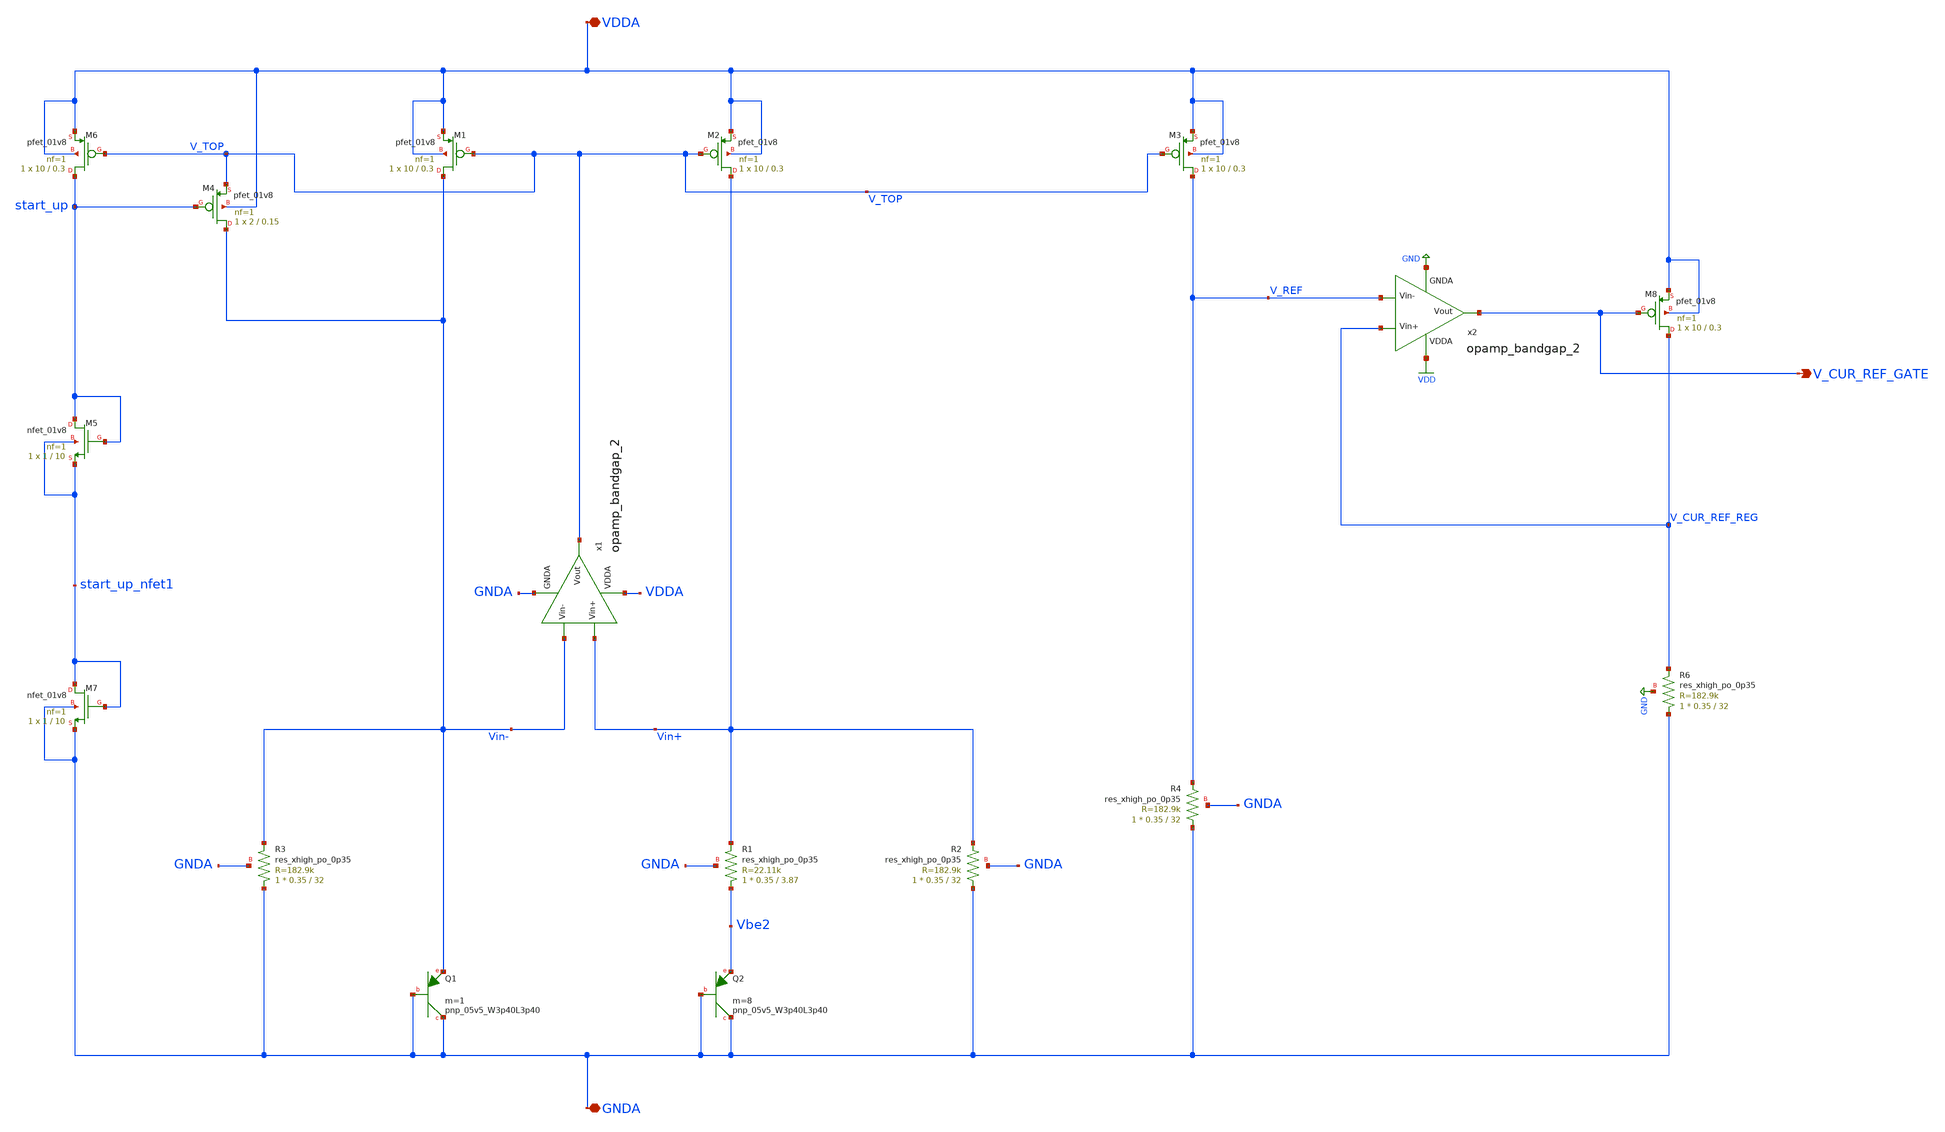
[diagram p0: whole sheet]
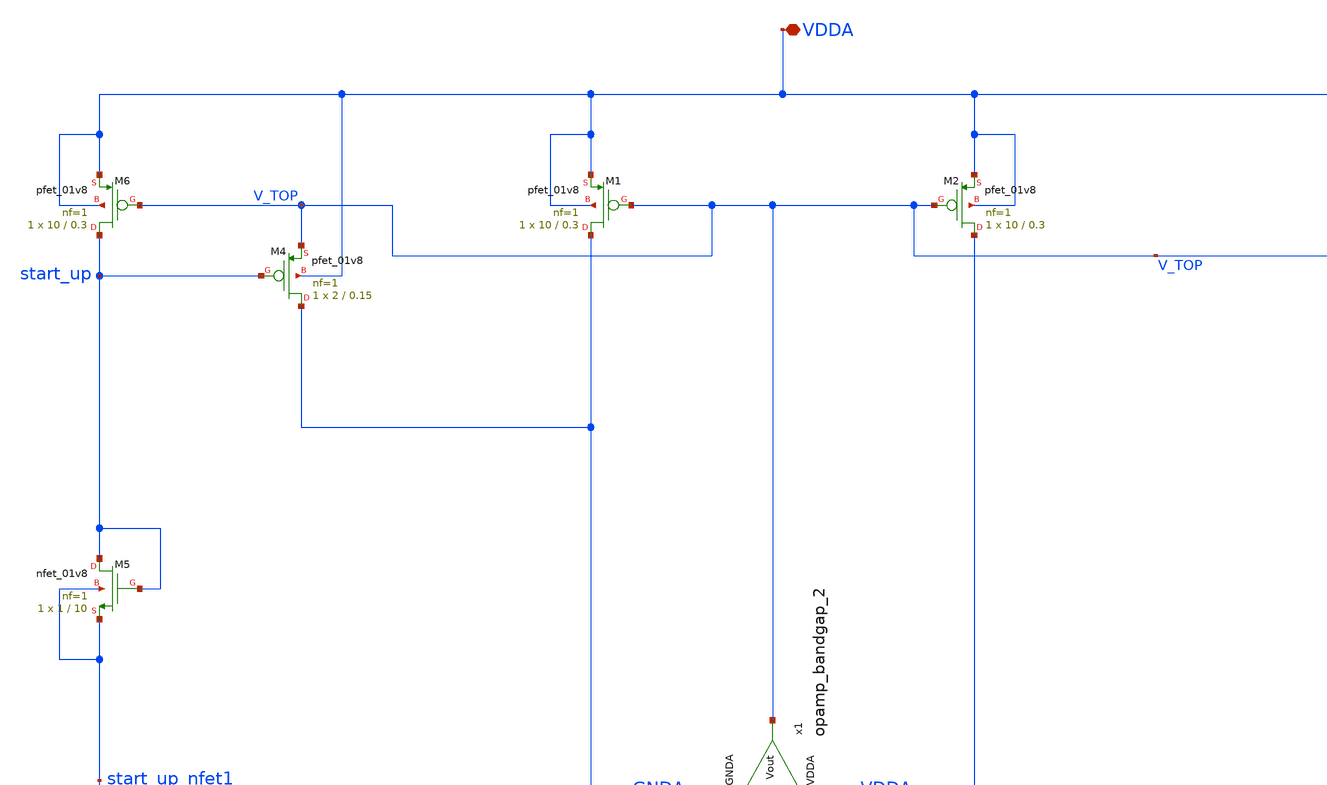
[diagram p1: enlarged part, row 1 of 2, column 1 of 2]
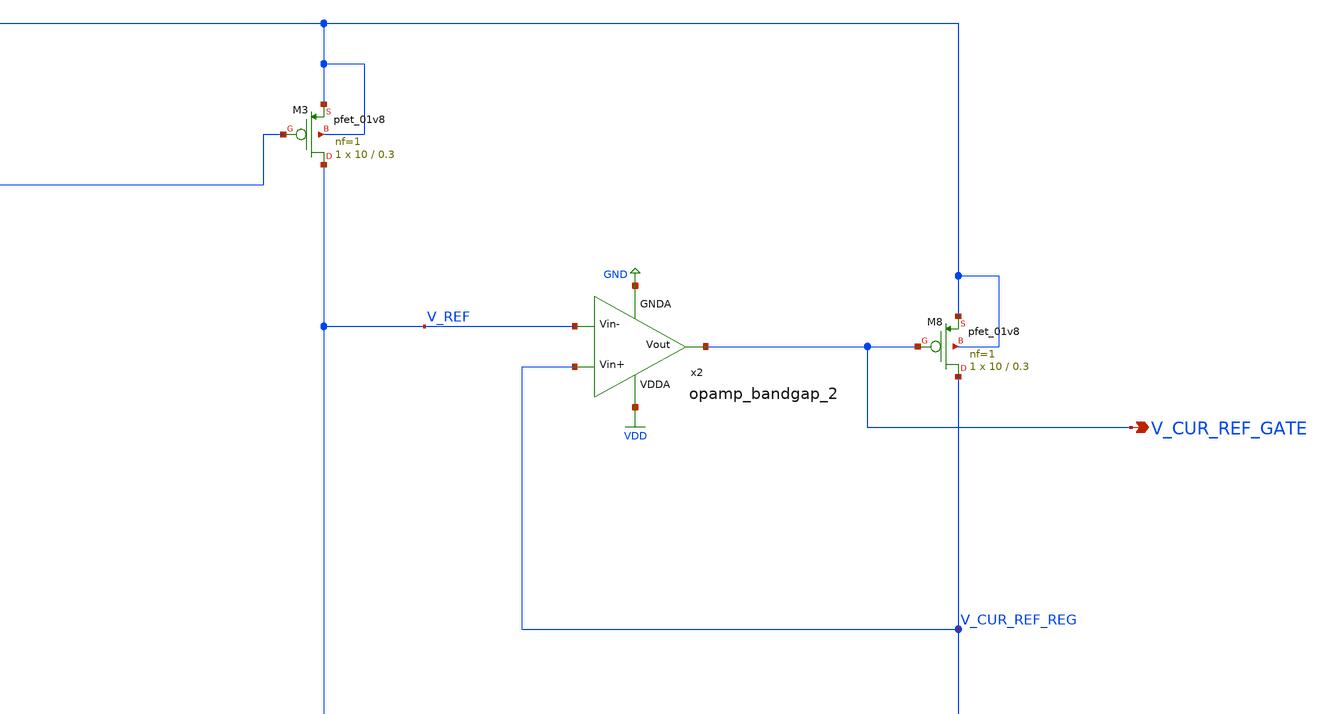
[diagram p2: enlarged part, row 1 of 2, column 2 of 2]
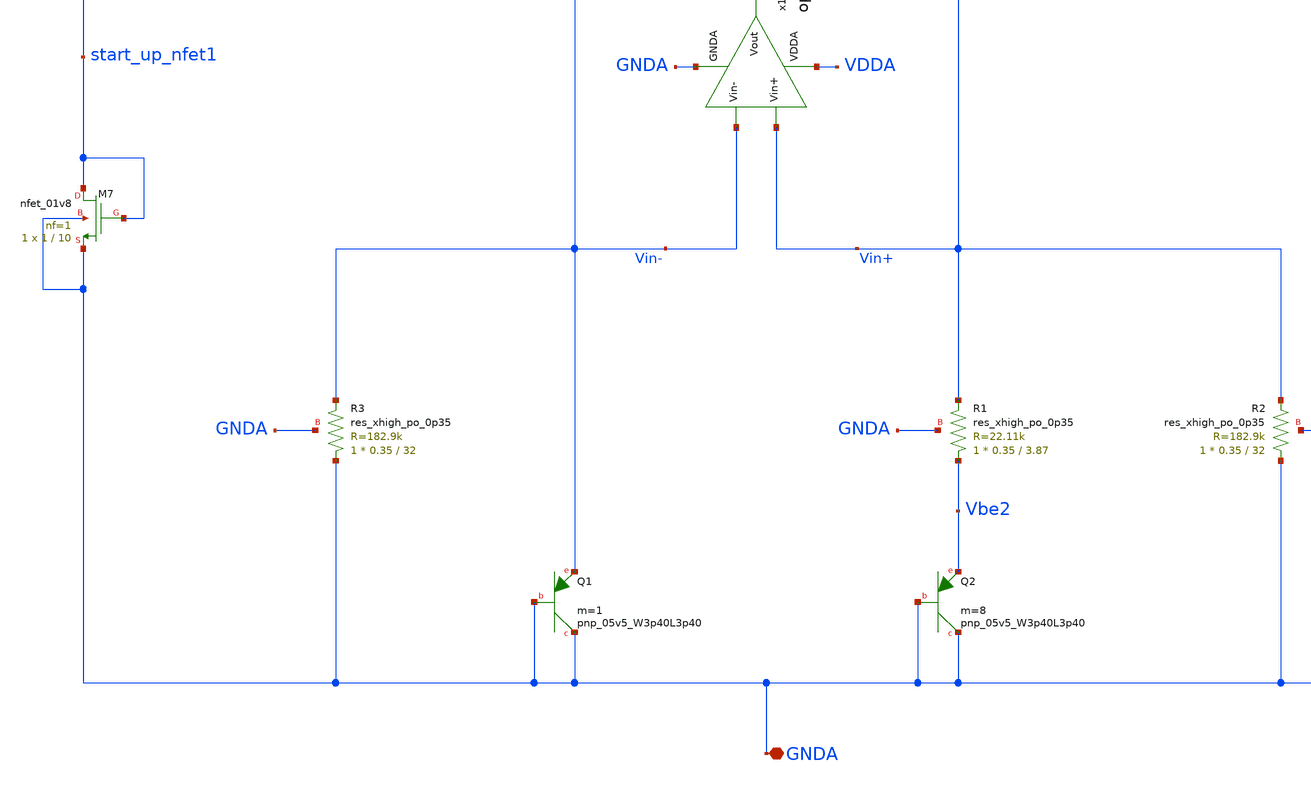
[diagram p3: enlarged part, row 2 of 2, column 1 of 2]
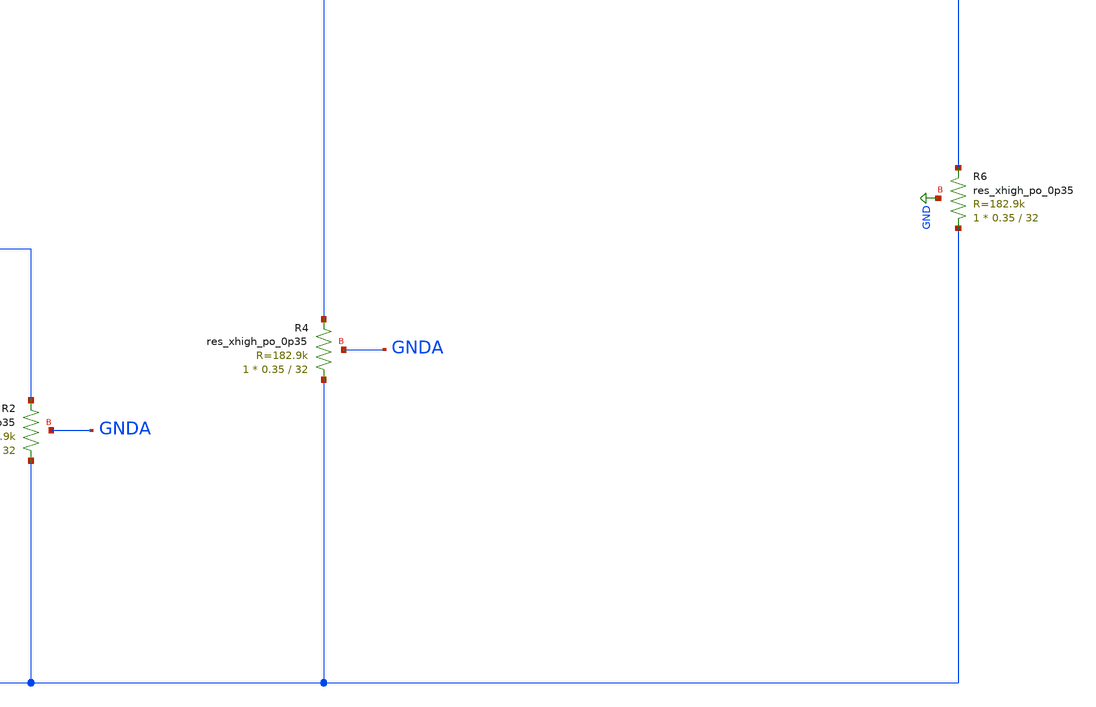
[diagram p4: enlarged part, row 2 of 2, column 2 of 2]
** sch_path: projects/bandgapref/xschem_ngspice/new_files/current_gen_5uA.sch
**.subckt current_gen_5uA VDDA GNDA V_CUR_REF_GATE
*.iopin VDDA
*.iopin GNDA
*.opin V_CUR_REF_GATE
XQ1 GNDA GNDA Vin- sky130_fd_pr__pnp_05v5_W3p40L3p40 m=1
XQ2 GNDA GNDA Vbe2 sky130_fd_pr__pnp_05v5_W3p40L3p40 m=8
XM1 Vin- V_TOP VDDA VDDA sky130_fd_pr__pfet_01v8 L=0.3 W=10 nf=1 ad='int((nf+1)/2) * W/nf * 0.29' as='int((nf+2)/2) * W/nf * 0.29'
+ pd='2*int((nf+1)/2) * (W/nf + 0.29)' ps='2*int((nf+2)/2) * (W/nf + 0.29)' nrd='0.29 / W' nrs='0.29 / W'
+ sa=0 sb=0 sd=0 mult=1 m=1
XM2 Vin+ V_TOP VDDA VDDA sky130_fd_pr__pfet_01v8 L=0.3 W=10 nf=1 ad='int((nf+1)/2) * W/nf * 0.29' as='int((nf+2)/2) * W/nf * 0.29'
+ pd='2*int((nf+1)/2) * (W/nf + 0.29)' ps='2*int((nf+2)/2) * (W/nf + 0.29)' nrd='0.29 / W' nrs='0.29 / W'
+ sa=0 sb=0 sd=0 mult=1 m=1
XM3 V_REF V_TOP VDDA VDDA sky130_fd_pr__pfet_01v8 L=0.3 W=10 nf=1 ad='int((nf+1)/2) * W/nf * 0.29' as='int((nf+2)/2) * W/nf * 0.29'
+ pd='2*int((nf+1)/2) * (W/nf + 0.29)' ps='2*int((nf+2)/2) * (W/nf + 0.29)' nrd='0.29 / W' nrs='0.29 / W'
+ sa=0 sb=0 sd=0 mult=1 m=1
XR1 Vbe2 Vin+ GNDA sky130_fd_pr__res_xhigh_po_0p35 L=3.87 mult=1 m=1
XR2 GNDA Vin+ GNDA sky130_fd_pr__res_xhigh_po_0p35 L=32 mult=1 m=1
XR3 GNDA Vin- GNDA sky130_fd_pr__res_xhigh_po_0p35 L=32 mult=1 m=1
XR4 GNDA V_REF GNDA sky130_fd_pr__res_xhigh_po_0p35 L=32 mult=1 m=1
XM5 start_up start_up start_up_nfet1 start_up_nfet1 sky130_fd_pr__nfet_01v8 L=10 W=1 nf=1 ad='int((nf+1)/2) * W/nf * 0.29'
+ as='int((nf+2)/2) * W/nf * 0.29' pd='2*int((nf+1)/2) * (W/nf + 0.29)' ps='2*int((nf+2)/2) * (W/nf + 0.29)'
+ nrd='0.29 / W' nrs='0.29 / W' sa=0 sb=0 sd=0 mult=1 m=1
XM6 start_up V_TOP VDDA VDDA sky130_fd_pr__pfet_01v8 L=0.3 W=10 nf=1 ad='int((nf+1)/2) * W/nf * 0.29'
+ as='int((nf+2)/2) * W/nf * 0.29' pd='2*int((nf+1)/2) * (W/nf + 0.29)' ps='2*int((nf+2)/2) * (W/nf + 0.29)'
+ nrd='0.29 / W' nrs='0.29 / W' sa=0 sb=0 sd=0 mult=1 m=1
XM4 Vin- start_up V_TOP VDDA sky130_fd_pr__pfet_01v8 L=0.15 W=2 nf=1 ad='int((nf+1)/2) * W/nf * 0.29'
+ as='int((nf+2)/2) * W/nf * 0.29' pd='2*int((nf+1)/2) * (W/nf + 0.29)' ps='2*int((nf+2)/2) * (W/nf + 0.29)'
+ nrd='0.29 / W' nrs='0.29 / W' sa=0 sb=0 sd=0 mult=1 m=1
x1 VDDA V_TOP Vin- Vin+ GNDA opamp_bandgap_2
XM7 start_up_nfet1 start_up_nfet1 GNDA GNDA sky130_fd_pr__nfet_01v8 L=10 W=1 nf=1 ad='int((nf+1)/2) * W/nf * 0.29'
+ as='int((nf+2)/2) * W/nf * 0.29' pd='2*int((nf+1)/2) * (W/nf + 0.29)' ps='2*int((nf+2)/2) * (W/nf + 0.29)'
+ nrd='0.29 / W' nrs='0.29 / W' sa=0 sb=0 sd=0 mult=1 m=1
x2 VDD V_CUR_REF_GATE V_REF V_CUR_REF_REG GND opamp_bandgap_2
XR6 GNDA V_CUR_REF_REG GND sky130_fd_pr__res_xhigh_po_0p35 L=32 mult=1 m=1
XM8 V_CUR_REF_REG V_CUR_REF_GATE VDDA VDDA sky130_fd_pr__pfet_01v8 L=0.3 W=10 nf=1 ad='int((nf+1)/2) * W/nf * 0.29'
+ as='int((nf+2)/2) * W/nf * 0.29' pd='2*int((nf+1)/2) * (W/nf + 0.29)' ps='2*int((nf+2)/2) * (W/nf + 0.29)'
+ nrd='0.29 / W' nrs='0.29 / W' sa=0 sb=0 sd=0 mult=1 m=1
**.ends

* expanding   symbol:  opamp_bandgap_2.sym # of pins=5
** sym_path: projects/bandgapref/xschem_ngspice/new_files/opamp_bandgap_2.sym
** sch_path: projects/bandgapref/xschem_ngspice/new_files/opamp_bandgap_2.sch
.subckt opamp_bandgap_2 VDDA Vout Vin- Vin+ GNDA
*.ipin Vin+
*.opin Vout
*.ipin Vin-
*.ipin GNDA
*.ipin VDDA
XM1 V_p VDDA GNDA GNDA sky130_fd_pr__nfet_01v8 L=10 W=5 nf=1 ad='int((nf+1)/2) * W/nf * 0.29' as='int((nf+2)/2) * W/nf * 0.29'
+ pd='2*int((nf+1)/2) * (W/nf + 0.29)' ps='2*int((nf+2)/2) * (W/nf + 0.29)' nrd='0.29 / W' nrs='0.29 / W'
+ sa=0 sb=0 sd=0 mult=1 m=1
XM2 V_mirror Vin- V_p GNDA sky130_fd_pr__nfet_01v8 L=0.2 W=5 nf=1 ad='int((nf+1)/2) * W/nf * 0.29' as='int((nf+2)/2) * W/nf * 0.29'
+ pd='2*int((nf+1)/2) * (W/nf + 0.29)' ps='2*int((nf+2)/2) * (W/nf + 0.29)' nrd='0.29 / W' nrs='0.29 / W'
+ sa=0 sb=0 sd=0 mult=1 m=1
XM3 1st_Vout Vin+ V_p GNDA sky130_fd_pr__nfet_01v8 L=0.2 W=5 nf=1 ad='int((nf+1)/2) * W/nf * 0.29' as='int((nf+2)/2) * W/nf * 0.29'
+ pd='2*int((nf+1)/2) * (W/nf + 0.29)' ps='2*int((nf+2)/2) * (W/nf + 0.29)' nrd='0.29 / W' nrs='0.29 / W'
+ sa=0 sb=0 sd=0 mult=1 m=1
XM5 V_mirror V_mirror VDDA VDDA sky130_fd_pr__pfet_01v8 L=0.2 W=10 nf=2 ad='int((nf+1)/2) * W/nf * 0.29'
+ as='int((nf+2)/2) * W/nf * 0.29' pd='2*int((nf+1)/2) * (W/nf + 0.29)' ps='2*int((nf+2)/2) * (W/nf + 0.29)'
+ nrd='0.29 / W' nrs='0.29 / W' sa=0 sb=0 sd=0 mult=1 m=1
XM6 1st_Vout V_mirror VDDA VDDA sky130_fd_pr__pfet_01v8 L=0.2 W=10 nf=2 ad='int((nf+1)/2) * W/nf * 0.29'
+ as='int((nf+2)/2) * W/nf * 0.29' pd='2*int((nf+1)/2) * (W/nf + 0.29)' ps='2*int((nf+2)/2) * (W/nf + 0.29)'
+ nrd='0.29 / W' nrs='0.29 / W' sa=0 sb=0 sd=0 mult=1 m=1
XM4 Vout VDDA GNDA GNDA sky130_fd_pr__nfet_01v8 L=10 W=5 nf=1 ad='int((nf+1)/2) * W/nf * 0.29' as='int((nf+2)/2) * W/nf * 0.29'
+ pd='2*int((nf+1)/2) * (W/nf + 0.29)' ps='2*int((nf+2)/2) * (W/nf + 0.29)' nrd='0.29 / W' nrs='0.29 / W'
+ sa=0 sb=0 sd=0 mult=1 m=1
XM7 Vout 1st_Vout VDDA VDDA sky130_fd_pr__pfet_01v8 L=0.2 W=10 nf=2 ad='int((nf+1)/2) * W/nf * 0.29'
+ as='int((nf+2)/2) * W/nf * 0.29' pd='2*int((nf+1)/2) * (W/nf + 0.29)' ps='2*int((nf+2)/2) * (W/nf + 0.29)'
+ nrd='0.29 / W' nrs='0.29 / W' sa=0 sb=0 sd=0 mult=1 m=1
.ends

.GLOBAL VDD
.GLOBAL GND
.end
